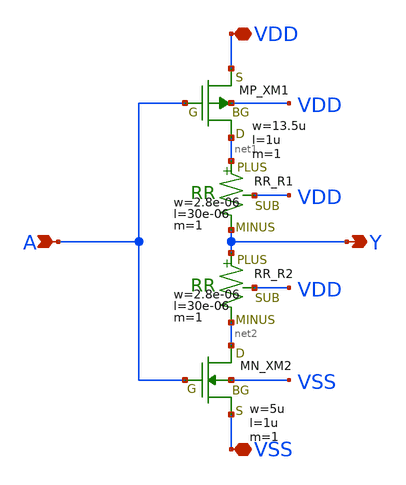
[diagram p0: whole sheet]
** sch_path: notebook/assets/schematics/src/inv_compact.sch
**.subckt inv_compact VDD VSS A Y
*.iopin VDD
*.iopin VSS
*.ipin A
*.opin Y
XXM1 net1 A VDD VDD PMOS w=13.5u l=1u nrd=0 nrs=0 m=1
XR1 net1 Y VDD F_RR w=2.8e-06 l=30e-06 R=1 tc1=0 tc2=0 m=1
XR2 Y net2 VDD F_RR w=2.8e-06 l=30e-06 R=1 tc1=0 tc2=0 m=1
XXM2 net2 A VSS VSS NMOS w=5u l=1u nrd=0 nrs=0 m=1
**.ends
.end
